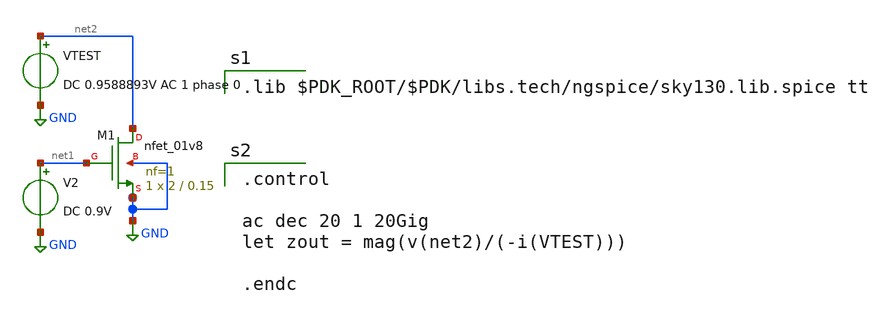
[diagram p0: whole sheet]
** sch_path: schematics/sky130_nmos_output_impedance.sch
**.subckt sky130_nmos_output_impedance
XM1 net2 net1 GND GND sky130_fd_pr__nfet_01v8 L=0.15 W=2 nf=1 ad='int((nf+1)/2) * W/nf * 0.29' as='int((nf+2)/2) * W/nf * 0.29'
+ pd='2*int((nf+1)/2) * (W/nf + 0.29)' ps='2*int((nf+2)/2) * (W/nf + 0.29)' nrd='0.29 / W' nrs='0.29 / W'
+ sa=0 sb=0 sd=0 mult=1 m=1
V2 net1 GND DC 0.9V
VTEST net2 GND DC 0.9588893V AC 1 phase 0
**** begin user architecture code

.lib $PDK_ROOT/$PDK/libs.tech/ngspice/sky130.lib.spice tt


.control

ac dec 20 1 20Gig
let zout = mag(v(net2)/(-i(VTEST)))

.endc

**** end user architecture code
**.ends
.GLOBAL GND
.end
